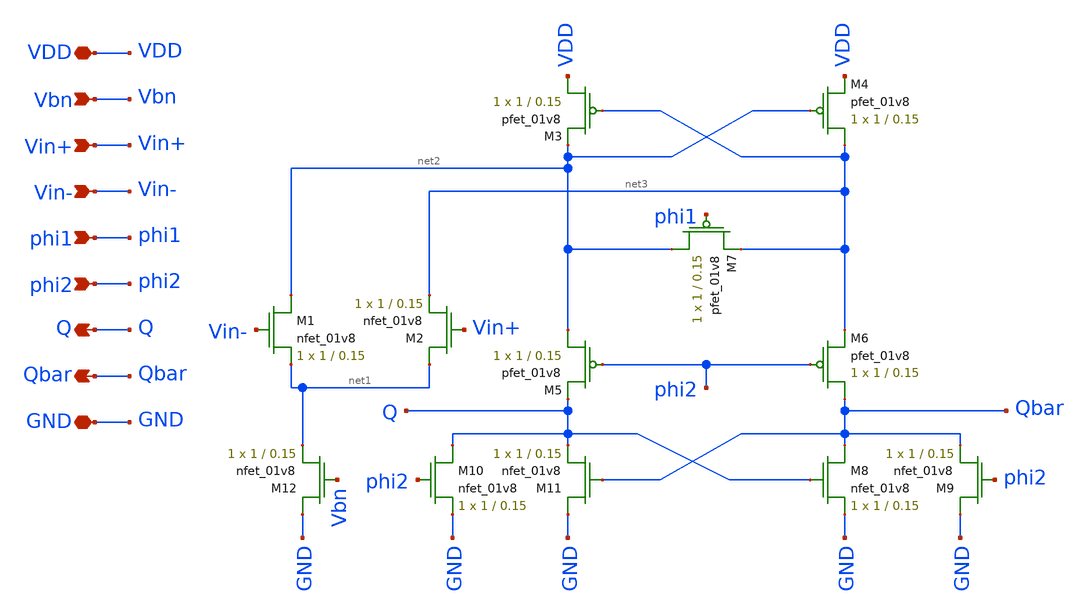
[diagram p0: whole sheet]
** sch_path: final/schematics/comparator.sch
**.subckt comparator Vin+ Vin- Vbn phi1 phi2 Q Qbar VDD GND
*.ipin Vin+
*.ipin Vin-
*.ipin Vbn
*.ipin phi1
*.ipin phi2
*.opin Q
*.opin Qbar
*.iopin VDD
*.iopin GND
XM1 net2 Vin- net1 GND sky130_fd_pr__nfet_01v8 L=0.15 W=1 nf=1 ad='int((nf+1)/2) * W/nf * 0.29' as='int((nf+2)/2) * W/nf * 0.29'
+ pd='2*int((nf+1)/2) * (W/nf + 0.29)' ps='2*int((nf+2)/2) * (W/nf + 0.29)' nrd='0.29 / W' nrs='0.29 / W'
+ sa=0 sb=0 sd=0 mult=1 m=1
XM2 net1 Vin+ net3 GND sky130_fd_pr__nfet_01v8 L=0.15 W=1 nf=1 ad='int((nf+1)/2) * W/nf * 0.29' as='int((nf+2)/2) * W/nf * 0.29'
+ pd='2*int((nf+1)/2) * (W/nf + 0.29)' ps='2*int((nf+2)/2) * (W/nf + 0.29)' nrd='0.29 / W' nrs='0.29 / W'
+ sa=0 sb=0 sd=0 mult=1 m=1
XM3 VDD net3 net2 VDD sky130_fd_pr__pfet_01v8 L=0.15 W=1 nf=1 ad='int((nf+1)/2) * W/nf * 0.29' as='int((nf+2)/2) * W/nf * 0.29'
+ pd='2*int((nf+1)/2) * (W/nf + 0.29)' ps='2*int((nf+2)/2) * (W/nf + 0.29)' nrd='0.29 / W' nrs='0.29 / W'
+ sa=0 sb=0 sd=0 mult=1 m=1
XM4 net3 net2 VDD VDD sky130_fd_pr__pfet_01v8 L=0.15 W=1 nf=1 ad='int((nf+1)/2) * W/nf * 0.29' as='int((nf+2)/2) * W/nf * 0.29'
+ pd='2*int((nf+1)/2) * (W/nf + 0.29)' ps='2*int((nf+2)/2) * (W/nf + 0.29)' nrd='0.29 / W' nrs='0.29 / W'
+ sa=0 sb=0 sd=0 mult=1 m=1
XM5 net2 phi2 Q VDD sky130_fd_pr__pfet_01v8 L=0.15 W=1 nf=1 ad='int((nf+1)/2) * W/nf * 0.29' as='int((nf+2)/2) * W/nf * 0.29'
+ pd='2*int((nf+1)/2) * (W/nf + 0.29)' ps='2*int((nf+2)/2) * (W/nf + 0.29)' nrd='0.29 / W' nrs='0.29 / W'
+ sa=0 sb=0 sd=0 mult=1 m=1
XM6 Qbar phi2 net3 VDD sky130_fd_pr__pfet_01v8 L=0.15 W=1 nf=1 ad='int((nf+1)/2) * W/nf * 0.29' as='int((nf+2)/2) * W/nf * 0.29'
+ pd='2*int((nf+1)/2) * (W/nf + 0.29)' ps='2*int((nf+2)/2) * (W/nf + 0.29)' nrd='0.29 / W' nrs='0.29 / W'
+ sa=0 sb=0 sd=0 mult=1 m=1
XM7 net2 phi1 net3 VDD sky130_fd_pr__pfet_01v8 L=0.15 W=1 nf=1 ad='int((nf+1)/2) * W/nf * 0.29' as='int((nf+2)/2) * W/nf * 0.29'
+ pd='2*int((nf+1)/2) * (W/nf + 0.29)' ps='2*int((nf+2)/2) * (W/nf + 0.29)' nrd='0.29 / W' nrs='0.29 / W'
+ sa=0 sb=0 sd=0 mult=1 m=1
XM8 Qbar Q GND GND sky130_fd_pr__nfet_01v8 L=0.15 W=1 nf=1 ad='int((nf+1)/2) * W/nf * 0.29' as='int((nf+2)/2) * W/nf * 0.29'
+ pd='2*int((nf+1)/2) * (W/nf + 0.29)' ps='2*int((nf+2)/2) * (W/nf + 0.29)' nrd='0.29 / W' nrs='0.29 / W'
+ sa=0 sb=0 sd=0 mult=1 m=1
XM9 GND phi2 Qbar GND sky130_fd_pr__nfet_01v8 L=0.15 W=1 nf=1 ad='int((nf+1)/2) * W/nf * 0.29' as='int((nf+2)/2) * W/nf * 0.29'
+ pd='2*int((nf+1)/2) * (W/nf + 0.29)' ps='2*int((nf+2)/2) * (W/nf + 0.29)' nrd='0.29 / W' nrs='0.29 / W'
+ sa=0 sb=0 sd=0 mult=1 m=1
XM10 Q phi2 GND GND sky130_fd_pr__nfet_01v8 L=0.15 W=1 nf=1 ad='int((nf+1)/2) * W/nf * 0.29' as='int((nf+2)/2) * W/nf * 0.29'
+ pd='2*int((nf+1)/2) * (W/nf + 0.29)' ps='2*int((nf+2)/2) * (W/nf + 0.29)' nrd='0.29 / W' nrs='0.29 / W'
+ sa=0 sb=0 sd=0 mult=1 m=1
XM11 GND Qbar Q GND sky130_fd_pr__nfet_01v8 L=0.15 W=1 nf=1 ad='int((nf+1)/2) * W/nf * 0.29' as='int((nf+2)/2) * W/nf * 0.29'
+ pd='2*int((nf+1)/2) * (W/nf + 0.29)' ps='2*int((nf+2)/2) * (W/nf + 0.29)' nrd='0.29 / W' nrs='0.29 / W'
+ sa=0 sb=0 sd=0 mult=1 m=1
XM12 GND Vbn net1 GND sky130_fd_pr__nfet_01v8 L=0.15 W=1 nf=1 ad='int((nf+1)/2) * W/nf * 0.29' as='int((nf+2)/2) * W/nf * 0.29'
+ pd='2*int((nf+1)/2) * (W/nf + 0.29)' ps='2*int((nf+2)/2) * (W/nf + 0.29)' nrd='0.29 / W' nrs='0.29 / W'
+ sa=0 sb=0 sd=0 mult=1 m=1
**.ends
.end
